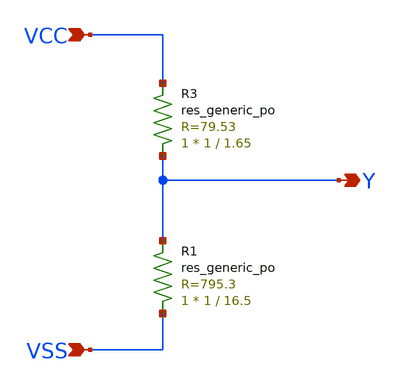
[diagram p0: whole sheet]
** sch_path: xschem/test/xschem/vDivider_3.sch
**.subckt vDivider_3 VCC VSS Y
*.ipin VCC
*.ipin VSS
*.opin Y
XR3 Y VCC sky130_fd_pr__res_generic_po W=1 L=1.65 m=1
XR1 VSS Y sky130_fd_pr__res_generic_po W=1 L=16.5 m=1
**.ends
.end
